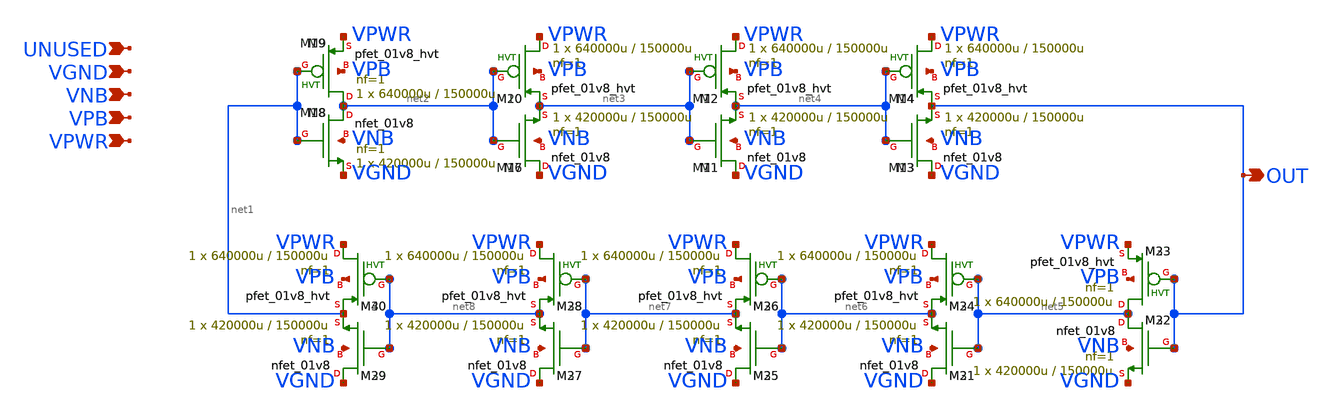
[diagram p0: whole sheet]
** sch_path: examples/ro/ro.sch
**.subckt ro VGND VNB VPB VPWR OUT UNUSED
*.ipin VGND
*.ipin VNB
*.ipin VPB
*.ipin VPWR
*.opin OUT
*.ipin UNUSED
XM16 VGND net2 net3 VNB sky130_fd_pr__nfet_01v8 L=150000u W=420000u nf=1 ad='int((1 + 1)/2) * 420000u / 1 * 0.29'
+ as='int((1 + 2)/2) * 420000u / 1 * 0.29' pd='2*int((1 + 1)/2) * (420000u / 1 + 0.29)' ps='2*int((1 + 2)/2) * (420000u / 1 + 0.29)'
+ nrd='0.29 / 420000u ' nrs='0.29 / 420000u ' sa=0 sb=0 sd=0 mult=1 m=1
XM18 net2 net1 VGND VNB sky130_fd_pr__nfet_01v8 L=150000u W=420000u nf=1 ad='int((1 + 1)/2) * 420000u / 1 * 0.29'
+ as='int((1 + 2)/2) * 420000u / 1 * 0.29' pd='2*int((1 + 1)/2) * (420000u / 1 + 0.29)' ps='2*int((1 + 2)/2) * (420000u / 1 + 0.29)'
+ nrd='0.29 / 420000u ' nrs='0.29 / 420000u ' sa=0 sb=0 sd=0 mult=1 m=1
XM19 net2 net1 VPWR VPB sky130_fd_pr__pfet_01v8_hvt L=150000u W=640000u nf=1 ad='int((1 + 1)/2) * 640000u / 1 * 0.29'
+ as='int((1 + 2)/2) * 640000u / 1 * 0.29' pd='2*int((1 + 1)/2) * (640000u / 1 + 0.29)' ps='2*int((1 + 2)/2) * (640000u / 1 + 0.29)'
+ nrd='0.29 / 640000u ' nrs='0.29 / 640000u ' sa=0 sb=0 sd=0 mult=1 m=1
XM20 VPWR net2 net3 VPB sky130_fd_pr__pfet_01v8_hvt L=150000u W=640000u nf=1 ad='int((1 + 1)/2) * 640000u / 1 * 0.29'
+ as='int((1 + 2)/2) * 640000u / 1 * 0.29' pd='2*int((1 + 1)/2) * (640000u / 1 + 0.29)' ps='2*int((1 + 2)/2) * (640000u / 1 + 0.29)'
+ nrd='0.29 / 640000u ' nrs='0.29 / 640000u ' sa=0 sb=0 sd=0 mult=1 m=1
XM1 VGND net3 net4 VNB sky130_fd_pr__nfet_01v8 L=150000u W=420000u nf=1 ad='int((1 + 1)/2) * 420000u / 1 * 0.29'
+ as='int((1 + 2)/2) * 420000u / 1 * 0.29' pd='2*int((1 + 1)/2) * (420000u / 1 + 0.29)' ps='2*int((1 + 2)/2) * (420000u / 1 + 0.29)'
+ nrd='0.29 / 420000u ' nrs='0.29 / 420000u ' sa=0 sb=0 sd=0 mult=1 m=1
XM2 VPWR net3 net4 VPB sky130_fd_pr__pfet_01v8_hvt L=150000u W=640000u nf=1 ad='int((1 + 1)/2) * 640000u / 1 * 0.29'
+ as='int((1 + 2)/2) * 640000u / 1 * 0.29' pd='2*int((1 + 1)/2) * (640000u / 1 + 0.29)' ps='2*int((1 + 2)/2) * (640000u / 1 + 0.29)'
+ nrd='0.29 / 640000u ' nrs='0.29 / 640000u ' sa=0 sb=0 sd=0 mult=1 m=1
XM3 VGND net4 OUT VNB sky130_fd_pr__nfet_01v8 L=150000u W=420000u nf=1 ad='int((1 + 1)/2) * 420000u / 1 * 0.29'
+ as='int((1 + 2)/2) * 420000u / 1 * 0.29' pd='2*int((1 + 1)/2) * (420000u / 1 + 0.29)' ps='2*int((1 + 2)/2) * (420000u / 1 + 0.29)'
+ nrd='0.29 / 420000u ' nrs='0.29 / 420000u ' sa=0 sb=0 sd=0 mult=1 m=1
XM4 VPWR net4 OUT VPB sky130_fd_pr__pfet_01v8_hvt L=150000u W=640000u nf=1 ad='int((1 + 1)/2) * 640000u / 1 * 0.29'
+ as='int((1 + 2)/2) * 640000u / 1 * 0.29' pd='2*int((1 + 1)/2) * (640000u / 1 + 0.29)' ps='2*int((1 + 2)/2) * (640000u / 1 + 0.29)'
+ nrd='0.29 / 640000u ' nrs='0.29 / 640000u ' sa=0 sb=0 sd=0 mult=1 m=1
XM7 VGND net2 net3 VNB sky130_fd_pr__nfet_01v8 L=150000u W=420000u nf=1 ad='int((1 + 1)/2) * 420000u / 1 * 0.29'
+ as='int((1 + 2)/2) * 420000u / 1 * 0.29' pd='2*int((1 + 1)/2) * (420000u / 1 + 0.29)' ps='2*int((1 + 2)/2) * (420000u / 1 + 0.29)'
+ nrd='0.29 / 420000u ' nrs='0.29 / 420000u ' sa=0 sb=0 sd=0 mult=1 m=1
XM8 net2 net1 VGND VNB sky130_fd_pr__nfet_01v8 L=150000u W=420000u nf=1 ad='int((1 + 1)/2) * 420000u / 1 * 0.29'
+ as='int((1 + 2)/2) * 420000u / 1 * 0.29' pd='2*int((1 + 1)/2) * (420000u / 1 + 0.29)' ps='2*int((1 + 2)/2) * (420000u / 1 + 0.29)'
+ nrd='0.29 / 420000u ' nrs='0.29 / 420000u ' sa=0 sb=0 sd=0 mult=1 m=1
XM9 net2 net1 VPWR VPB sky130_fd_pr__pfet_01v8_hvt L=150000u W=640000u nf=1 ad='int((1 + 1)/2) * 640000u / 1 * 0.29'
+ as='int((1 + 2)/2) * 640000u / 1 * 0.29' pd='2*int((1 + 1)/2) * (640000u / 1 + 0.29)' ps='2*int((1 + 2)/2) * (640000u / 1 + 0.29)'
+ nrd='0.29 / 640000u ' nrs='0.29 / 640000u ' sa=0 sb=0 sd=0 mult=1 m=1
XM10 VPWR net2 net3 VPB sky130_fd_pr__pfet_01v8_hvt L=150000u W=640000u nf=1 ad='int((1 + 1)/2) * 640000u / 1 * 0.29'
+ as='int((1 + 2)/2) * 640000u / 1 * 0.29' pd='2*int((1 + 1)/2) * (640000u / 1 + 0.29)' ps='2*int((1 + 2)/2) * (640000u / 1 + 0.29)'
+ nrd='0.29 / 640000u ' nrs='0.29 / 640000u ' sa=0 sb=0 sd=0 mult=1 m=1
XM11 VGND net3 net4 VNB sky130_fd_pr__nfet_01v8 L=150000u W=420000u nf=1 ad='int((1 + 1)/2) * 420000u / 1 * 0.29'
+ as='int((1 + 2)/2) * 420000u / 1 * 0.29' pd='2*int((1 + 1)/2) * (420000u / 1 + 0.29)' ps='2*int((1 + 2)/2) * (420000u / 1 + 0.29)'
+ nrd='0.29 / 420000u ' nrs='0.29 / 420000u ' sa=0 sb=0 sd=0 mult=1 m=1
XM12 VPWR net3 net4 VPB sky130_fd_pr__pfet_01v8_hvt L=150000u W=640000u nf=1 ad='int((1 + 1)/2) * 640000u / 1 * 0.29'
+ as='int((1 + 2)/2) * 640000u / 1 * 0.29' pd='2*int((1 + 1)/2) * (640000u / 1 + 0.29)' ps='2*int((1 + 2)/2) * (640000u / 1 + 0.29)'
+ nrd='0.29 / 640000u ' nrs='0.29 / 640000u ' sa=0 sb=0 sd=0 mult=1 m=1
XM13 VGND net4 OUT VNB sky130_fd_pr__nfet_01v8 L=150000u W=420000u nf=1 ad='int((1 + 1)/2) * 420000u / 1 * 0.29'
+ as='int((1 + 2)/2) * 420000u / 1 * 0.29' pd='2*int((1 + 1)/2) * (420000u / 1 + 0.29)' ps='2*int((1 + 2)/2) * (420000u / 1 + 0.29)'
+ nrd='0.29 / 420000u ' nrs='0.29 / 420000u ' sa=0 sb=0 sd=0 mult=1 m=1
XM14 VPWR net4 OUT VPB sky130_fd_pr__pfet_01v8_hvt L=150000u W=640000u nf=1 ad='int((1 + 1)/2) * 640000u / 1 * 0.29'
+ as='int((1 + 2)/2) * 640000u / 1 * 0.29' pd='2*int((1 + 1)/2) * (640000u / 1 + 0.29)' ps='2*int((1 + 2)/2) * (640000u / 1 + 0.29)'
+ nrd='0.29 / 640000u ' nrs='0.29 / 640000u ' sa=0 sb=0 sd=0 mult=1 m=1
XM21 VGND net5 net6 VNB sky130_fd_pr__nfet_01v8 L=150000u W=420000u nf=1 ad='int((1 + 1)/2) * 420000u / 1 * 0.29'
+ as='int((1 + 2)/2) * 420000u / 1 * 0.29' pd='2*int((1 + 1)/2) * (420000u / 1 + 0.29)' ps='2*int((1 + 2)/2) * (420000u / 1 + 0.29)'
+ nrd='0.29 / 420000u ' nrs='0.29 / 420000u ' sa=0 sb=0 sd=0 mult=1 m=1
XM22 net5 OUT VGND VNB sky130_fd_pr__nfet_01v8 L=150000u W=420000u nf=1 ad='int((1 + 1)/2) * 420000u / 1 * 0.29'
+ as='int((1 + 2)/2) * 420000u / 1 * 0.29' pd='2*int((1 + 1)/2) * (420000u / 1 + 0.29)' ps='2*int((1 + 2)/2) * (420000u / 1 + 0.29)'
+ nrd='0.29 / 420000u ' nrs='0.29 / 420000u ' sa=0 sb=0 sd=0 mult=1 m=1
XM23 net5 OUT VPWR VPB sky130_fd_pr__pfet_01v8_hvt L=150000u W=640000u nf=1 ad='int((1 + 1)/2) * 640000u / 1 * 0.29'
+ as='int((1 + 2)/2) * 640000u / 1 * 0.29' pd='2*int((1 + 1)/2) * (640000u / 1 + 0.29)' ps='2*int((1 + 2)/2) * (640000u / 1 + 0.29)'
+ nrd='0.29 / 640000u ' nrs='0.29 / 640000u ' sa=0 sb=0 sd=0 mult=1 m=1
XM24 VPWR net5 net6 VPB sky130_fd_pr__pfet_01v8_hvt L=150000u W=640000u nf=1 ad='int((1 + 1)/2) * 640000u / 1 * 0.29'
+ as='int((1 + 2)/2) * 640000u / 1 * 0.29' pd='2*int((1 + 1)/2) * (640000u / 1 + 0.29)' ps='2*int((1 + 2)/2) * (640000u / 1 + 0.29)'
+ nrd='0.29 / 640000u ' nrs='0.29 / 640000u ' sa=0 sb=0 sd=0 mult=1 m=1
XM25 VGND net6 net7 VNB sky130_fd_pr__nfet_01v8 L=150000u W=420000u nf=1 ad='int((1 + 1)/2) * 420000u / 1 * 0.29'
+ as='int((1 + 2)/2) * 420000u / 1 * 0.29' pd='2*int((1 + 1)/2) * (420000u / 1 + 0.29)' ps='2*int((1 + 2)/2) * (420000u / 1 + 0.29)'
+ nrd='0.29 / 420000u ' nrs='0.29 / 420000u ' sa=0 sb=0 sd=0 mult=1 m=1
XM26 VPWR net6 net7 VPB sky130_fd_pr__pfet_01v8_hvt L=150000u W=640000u nf=1 ad='int((1 + 1)/2) * 640000u / 1 * 0.29'
+ as='int((1 + 2)/2) * 640000u / 1 * 0.29' pd='2*int((1 + 1)/2) * (640000u / 1 + 0.29)' ps='2*int((1 + 2)/2) * (640000u / 1 + 0.29)'
+ nrd='0.29 / 640000u ' nrs='0.29 / 640000u ' sa=0 sb=0 sd=0 mult=1 m=1
XM27 VGND net7 net8 VNB sky130_fd_pr__nfet_01v8 L=150000u W=420000u nf=1 ad='int((1 + 1)/2) * 420000u / 1 * 0.29'
+ as='int((1 + 2)/2) * 420000u / 1 * 0.29' pd='2*int((1 + 1)/2) * (420000u / 1 + 0.29)' ps='2*int((1 + 2)/2) * (420000u / 1 + 0.29)'
+ nrd='0.29 / 420000u ' nrs='0.29 / 420000u ' sa=0 sb=0 sd=0 mult=1 m=1
XM28 VPWR net7 net8 VPB sky130_fd_pr__pfet_01v8_hvt L=150000u W=640000u nf=1 ad='int((1 + 1)/2) * 640000u / 1 * 0.29'
+ as='int((1 + 2)/2) * 640000u / 1 * 0.29' pd='2*int((1 + 1)/2) * (640000u / 1 + 0.29)' ps='2*int((1 + 2)/2) * (640000u / 1 + 0.29)'
+ nrd='0.29 / 640000u ' nrs='0.29 / 640000u ' sa=0 sb=0 sd=0 mult=1 m=1
XM29 VGND net8 net1 VNB sky130_fd_pr__nfet_01v8 L=150000u W=420000u nf=1 ad='int((1 + 1)/2) * 420000u / 1 * 0.29'
+ as='int((1 + 2)/2) * 420000u / 1 * 0.29' pd='2*int((1 + 1)/2) * (420000u / 1 + 0.29)' ps='2*int((1 + 2)/2) * (420000u / 1 + 0.29)'
+ nrd='0.29 / 420000u ' nrs='0.29 / 420000u ' sa=0 sb=0 sd=0 mult=1 m=1
XM30 VPWR net8 net1 VPB sky130_fd_pr__pfet_01v8_hvt L=150000u W=640000u nf=1 ad='int((1 + 1)/2) * 640000u / 1 * 0.29'
+ as='int((1 + 2)/2) * 640000u / 1 * 0.29' pd='2*int((1 + 1)/2) * (640000u / 1 + 0.29)' ps='2*int((1 + 2)/2) * (640000u / 1 + 0.29)'
+ nrd='0.29 / 640000u ' nrs='0.29 / 640000u ' sa=0 sb=0 sd=0 mult=1 m=1
XM31 VGND net5 net6 VNB sky130_fd_pr__nfet_01v8 L=150000u W=420000u nf=1 ad='int((1 + 1)/2) * 420000u / 1 * 0.29'
+ as='int((1 + 2)/2) * 420000u / 1 * 0.29' pd='2*int((1 + 1)/2) * (420000u / 1 + 0.29)' ps='2*int((1 + 2)/2) * (420000u / 1 + 0.29)'
+ nrd='0.29 / 420000u ' nrs='0.29 / 420000u ' sa=0 sb=0 sd=0 mult=1 m=1
XM32 net5 OUT VGND VNB sky130_fd_pr__nfet_01v8 L=150000u W=420000u nf=1 ad='int((1 + 1)/2) * 420000u / 1 * 0.29'
+ as='int((1 + 2)/2) * 420000u / 1 * 0.29' pd='2*int((1 + 1)/2) * (420000u / 1 + 0.29)' ps='2*int((1 + 2)/2) * (420000u / 1 + 0.29)'
+ nrd='0.29 / 420000u ' nrs='0.29 / 420000u ' sa=0 sb=0 sd=0 mult=1 m=1
XM33 net5 OUT VPWR VPB sky130_fd_pr__pfet_01v8_hvt L=150000u W=640000u nf=1 ad='int((1 + 1)/2) * 640000u / 1 * 0.29'
+ as='int((1 + 2)/2) * 640000u / 1 * 0.29' pd='2*int((1 + 1)/2) * (640000u / 1 + 0.29)' ps='2*int((1 + 2)/2) * (640000u / 1 + 0.29)'
+ nrd='0.29 / 640000u ' nrs='0.29 / 640000u ' sa=0 sb=0 sd=0 mult=1 m=1
XM34 VPWR net5 net6 VPB sky130_fd_pr__pfet_01v8_hvt L=150000u W=640000u nf=1 ad='int((1 + 1)/2) * 640000u / 1 * 0.29'
+ as='int((1 + 2)/2) * 640000u / 1 * 0.29' pd='2*int((1 + 1)/2) * (640000u / 1 + 0.29)' ps='2*int((1 + 2)/2) * (640000u / 1 + 0.29)'
+ nrd='0.29 / 640000u ' nrs='0.29 / 640000u ' sa=0 sb=0 sd=0 mult=1 m=1
XM35 VGND net6 net7 VNB sky130_fd_pr__nfet_01v8 L=150000u W=420000u nf=1 ad='int((1 + 1)/2) * 420000u / 1 * 0.29'
+ as='int((1 + 2)/2) * 420000u / 1 * 0.29' pd='2*int((1 + 1)/2) * (420000u / 1 + 0.29)' ps='2*int((1 + 2)/2) * (420000u / 1 + 0.29)'
+ nrd='0.29 / 420000u ' nrs='0.29 / 420000u ' sa=0 sb=0 sd=0 mult=1 m=1
XM36 VPWR net6 net7 VPB sky130_fd_pr__pfet_01v8_hvt L=150000u W=640000u nf=1 ad='int((1 + 1)/2) * 640000u / 1 * 0.29'
+ as='int((1 + 2)/2) * 640000u / 1 * 0.29' pd='2*int((1 + 1)/2) * (640000u / 1 + 0.29)' ps='2*int((1 + 2)/2) * (640000u / 1 + 0.29)'
+ nrd='0.29 / 640000u ' nrs='0.29 / 640000u ' sa=0 sb=0 sd=0 mult=1 m=1
XM37 VGND net7 net8 VNB sky130_fd_pr__nfet_01v8 L=150000u W=420000u nf=1 ad='int((1 + 1)/2) * 420000u / 1 * 0.29'
+ as='int((1 + 2)/2) * 420000u / 1 * 0.29' pd='2*int((1 + 1)/2) * (420000u / 1 + 0.29)' ps='2*int((1 + 2)/2) * (420000u / 1 + 0.29)'
+ nrd='0.29 / 420000u ' nrs='0.29 / 420000u ' sa=0 sb=0 sd=0 mult=1 m=1
XM38 VPWR net7 net8 VPB sky130_fd_pr__pfet_01v8_hvt L=150000u W=640000u nf=1 ad='int((1 + 1)/2) * 640000u / 1 * 0.29'
+ as='int((1 + 2)/2) * 640000u / 1 * 0.29' pd='2*int((1 + 1)/2) * (640000u / 1 + 0.29)' ps='2*int((1 + 2)/2) * (640000u / 1 + 0.29)'
+ nrd='0.29 / 640000u ' nrs='0.29 / 640000u ' sa=0 sb=0 sd=0 mult=1 m=1
XM39 VGND net8 net1 VNB sky130_fd_pr__nfet_01v8 L=150000u W=420000u nf=1 ad='int((1 + 1)/2) * 420000u / 1 * 0.29'
+ as='int((1 + 2)/2) * 420000u / 1 * 0.29' pd='2*int((1 + 1)/2) * (420000u / 1 + 0.29)' ps='2*int((1 + 2)/2) * (420000u / 1 + 0.29)'
+ nrd='0.29 / 420000u ' nrs='0.29 / 420000u ' sa=0 sb=0 sd=0 mult=1 m=1
XM40 VPWR net8 net1 VPB sky130_fd_pr__pfet_01v8_hvt L=150000u W=640000u nf=1 ad='int((1 + 1)/2) * 640000u / 1 * 0.29'
+ as='int((1 + 2)/2) * 640000u / 1 * 0.29' pd='2*int((1 + 1)/2) * (640000u / 1 + 0.29)' ps='2*int((1 + 2)/2) * (640000u / 1 + 0.29)'
+ nrd='0.29 / 640000u ' nrs='0.29 / 640000u ' sa=0 sb=0 sd=0 mult=1 m=1
**.ends
.end
